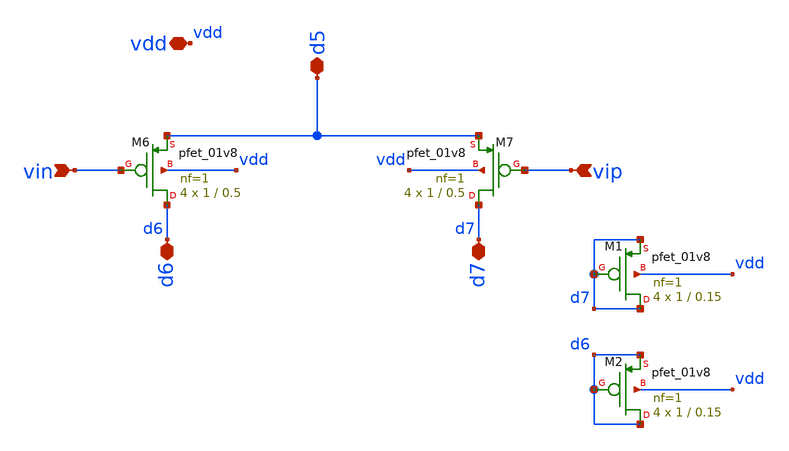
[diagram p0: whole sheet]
** sch_path: mag/pmos_dif.sch
**.subckt pmos_dif vin vip vdd d6 d5 d7
*.ipin vin
*.ipin vip
*.iopin vdd
*.iopin d6
*.iopin d5
*.iopin d7
XM6 d6 vin d5 vdd sky130_fd_pr__pfet_01v8 L=0.5 W=1 nf=1 ad='int((nf+1)/2) * W/nf * 0.29' as='int((nf+2)/2) * W/nf * 0.29'
+ pd='2*int((nf+1)/2) * (W/nf + 0.29)' ps='2*int((nf+2)/2) * (W/nf + 0.29)' nrd='0.29 / W' nrs='0.29 / W'
+ sa=0 sb=0 sd=0 mult=4 m=4
XM7 d7 vip d5 vdd sky130_fd_pr__pfet_01v8 L=0.5 W=1 nf=1 ad='int((nf+1)/2) * W/nf * 0.29' as='int((nf+2)/2) * W/nf * 0.29'
+ pd='2*int((nf+1)/2) * (W/nf + 0.29)' ps='2*int((nf+2)/2) * (W/nf + 0.29)' nrd='0.29 / W' nrs='0.29 / W'
+ sa=0 sb=0 sd=0 mult=4 m=4
XM1 d7 d7 d7 vdd sky130_fd_pr__pfet_01v8 L=0.15 W=1 nf=1 ad='int((nf+1)/2) * W/nf * 0.29' as='int((nf+2)/2) * W/nf * 0.29'
+ pd='2*int((nf+1)/2) * (W/nf + 0.29)' ps='2*int((nf+2)/2) * (W/nf + 0.29)' nrd='0.29 / W' nrs='0.29 / W'
+ sa=0 sb=0 sd=0 mult=4 m=4
XM2 d6 d6 d6 vdd sky130_fd_pr__pfet_01v8 L=0.15 W=1 nf=1 ad='int((nf+1)/2) * W/nf * 0.29' as='int((nf+2)/2) * W/nf * 0.29'
+ pd='2*int((nf+1)/2) * (W/nf + 0.29)' ps='2*int((nf+2)/2) * (W/nf + 0.29)' nrd='0.29 / W' nrs='0.29 / W'
+ sa=0 sb=0 sd=0 mult=4 m=4
**.ends
.end
